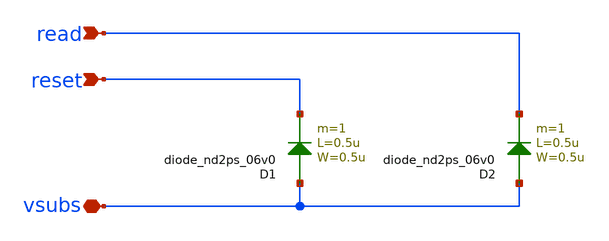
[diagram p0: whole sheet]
** sch_path: xschem/ip_pixel_frame_right.sch
**.subckt ip_pixel_frame_right read reset vsubs
*.ipin read
*.ipin reset
*.iopin vsubs
D1 vsubs reset diode_nd2ps_06v0 area='0.5u * 0.5u ' pj='2*0.5u + 2*0.5u ' m=1
D2 vsubs read diode_nd2ps_06v0 area='0.5u * 0.5u ' pj='2*0.5u + 2*0.5u ' m=1
**.ends
.end
